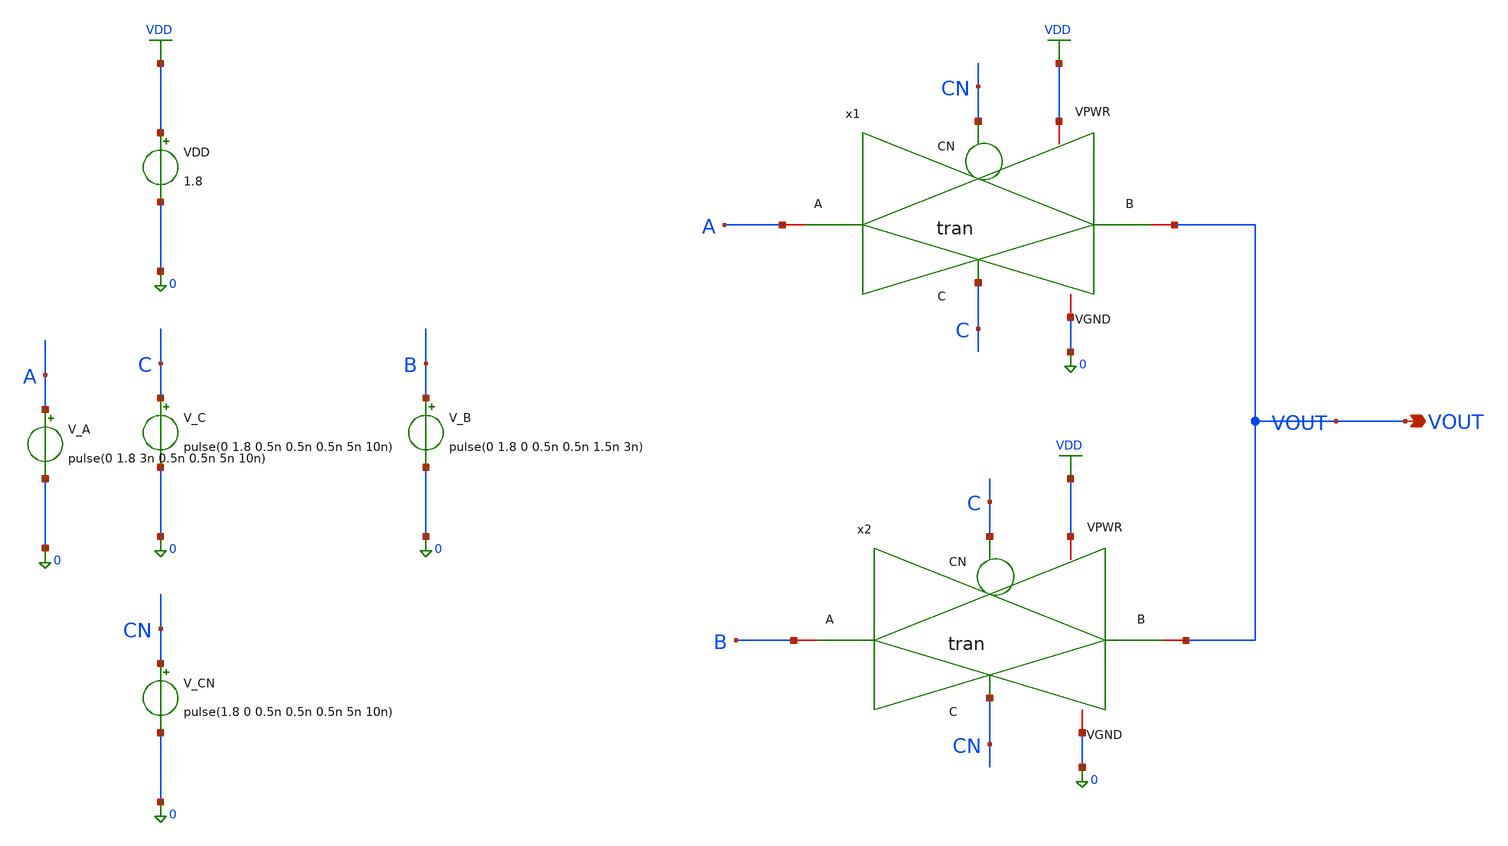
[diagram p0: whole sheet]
** sch_path: latch/tran_tb.sch
**.subckt tran_tb VOUT
*.opin VOUT
x1 CN VDD VOUT A 0 C tran
VDD VDD 0 1.8
V_C C 0 pulse(0 1.8 0.5n 0.5n 0.5n 5n 10n)
V_CN CN 0 pulse(1.8 0 0.5n 0.5n 0.5n 5n 10n)
V_A A 0 pulse(0 1.8 3n 0.5n 0.5n 5n 10n)
x2 C VDD VOUT B 0 CN tran
V_B B 0 pulse(0 1.8 0 0.5n 0.5n 1.5n 3n)
**** begin user architecture code

** opencircuitdesign pdks install
.lib $::SKYWATER_MODELS/sky130.lib.spice tt



.tran 0.01n 15n
.control
  save all
    run
    write /home/sushanth/.xschem/simulations/output.raw
  end
.endc


**** end user architecture code
**.ends

* expanding   symbol:  tran.sym # of pins=6
** sym_path: trans/tran.sym
** sch_path: trans/tran.sch
.subckt tran CN VPWR B A VGND C
*.iopin A
*.iopin B
*.iopin VPWR
*.iopin VGND
*.ipin C
*.ipin CN
XM1 A C B VGND sky130_fd_pr__nfet_01v8 L=0.15 W=0.65 nf=1 ad='int((1 + 1)/2) * 0.65 / 1 * 0.29' as='int((1 + 2)/2) * 0.65 / 1 * 0.29'
+ pd='2*int((1 + 1)/2) * (0.65 / 1 + 0.29)' ps='2*int((1 + 2)/2) * (0.65 / 1 + 0.29)' nrd='0.29 / 0.65 '
+ nrs='0.29 / 0.65 ' sa=0 sb=0 sd=0 mult=1 m=1
XM2 A CN B VPWR sky130_fd_pr__pfet_01v8 L=0.15 W=1 nf=1 ad='int((1 + 1)/2) * 1 / 1 * 0.29' as='int((1 + 2)/2) * 1 / 1 * 0.29'
+ pd='2*int((1 + 1)/2) * (1 / 1 + 0.29)' ps='2*int((1 + 2)/2) * (1 / 1 + 0.29)' nrd='0.29 / 1 ' nrs='0.29 / 1 '
+ sa=0 sb=0 sd=0 mult=1 m=1
.ends

.GLOBAL VDD
.end
